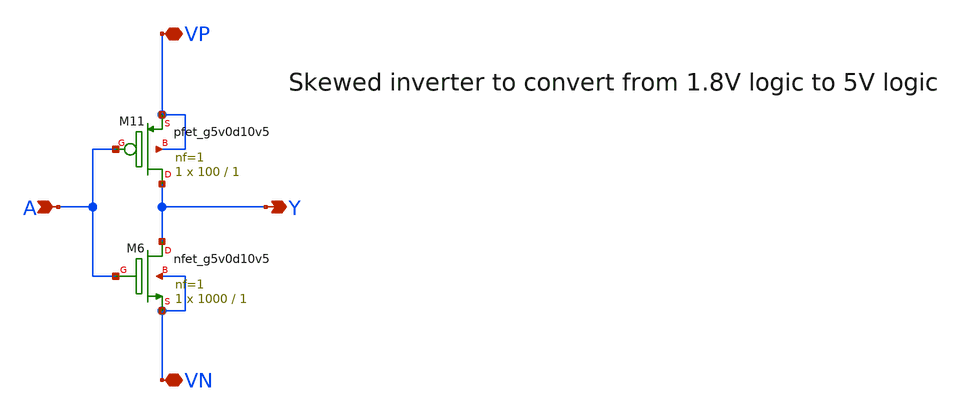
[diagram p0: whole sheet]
** sch_path: ADC/4bit_C2C/MagicAndSpice/old_inverter_1v8_to_5v.sch
**.subckt old_inverter_1v8_to_5v A Y VP VN
*.ipin A
*.opin Y
*.iopin VP
*.iopin VN
XM6 Y A VN VN sky130_fd_pr__nfet_g5v0d10v5 L=1 W=1000 nf=1 ad='int((nf+1)/2) * W/nf * 0.29' as='int((nf+2)/2) * W/nf * 0.29'
+ pd='2*int((nf+1)/2) * (W/nf + 0.29)' ps='2*int((nf+2)/2) * (W/nf + 0.29)' nrd='0.29 / W' nrs='0.29 / W'
+ sa=0 sb=0 sd=0 mult=1 m=1
XM11 Y A VP VP sky130_fd_pr__pfet_g5v0d10v5 L=1 W=100 nf=1 ad='int((nf+1)/2) * W/nf * 0.29' as='int((nf+2)/2) * W/nf * 0.29'
+ pd='2*int((nf+1)/2) * (W/nf + 0.29)' ps='2*int((nf+2)/2) * (W/nf + 0.29)' nrd='0.29 / W' nrs='0.29 / W'
+ sa=0 sb=0 sd=0 mult=1 m=1
**.ends
.end
